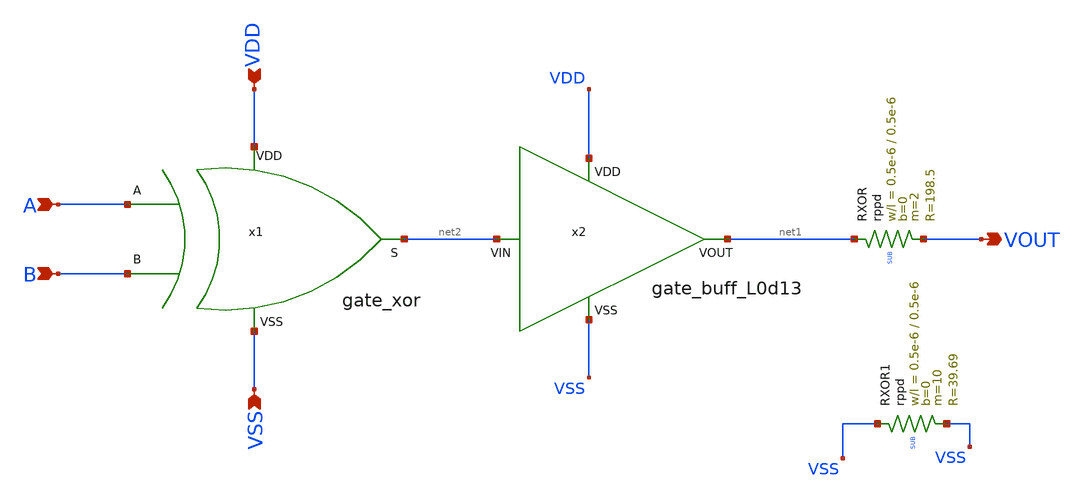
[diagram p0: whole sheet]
** sch_path: work/integrator_phasedetector/xschem/integrator_phasedetector.sch
**.subckt integrator_phasedetector A B VSS VDD VOUT
*.ipin A
*.ipin B
*.ipin VSS
*.ipin VDD
*.opin VOUT
x1 VDD net2 B A VSS gate_xor
x2 VDD net2 net1 VSS gate_buff_L0d13
XRXOR net1 VOUT SUB rppd w=0.5e-6 l=0.5e-6 m=2 b=0 mm_ok=1
XRXOR1 VSS VSS SUB rppd w=0.5e-6 l=0.5e-6 m=10 b=0 mm_ok=1
**.ends
.end
